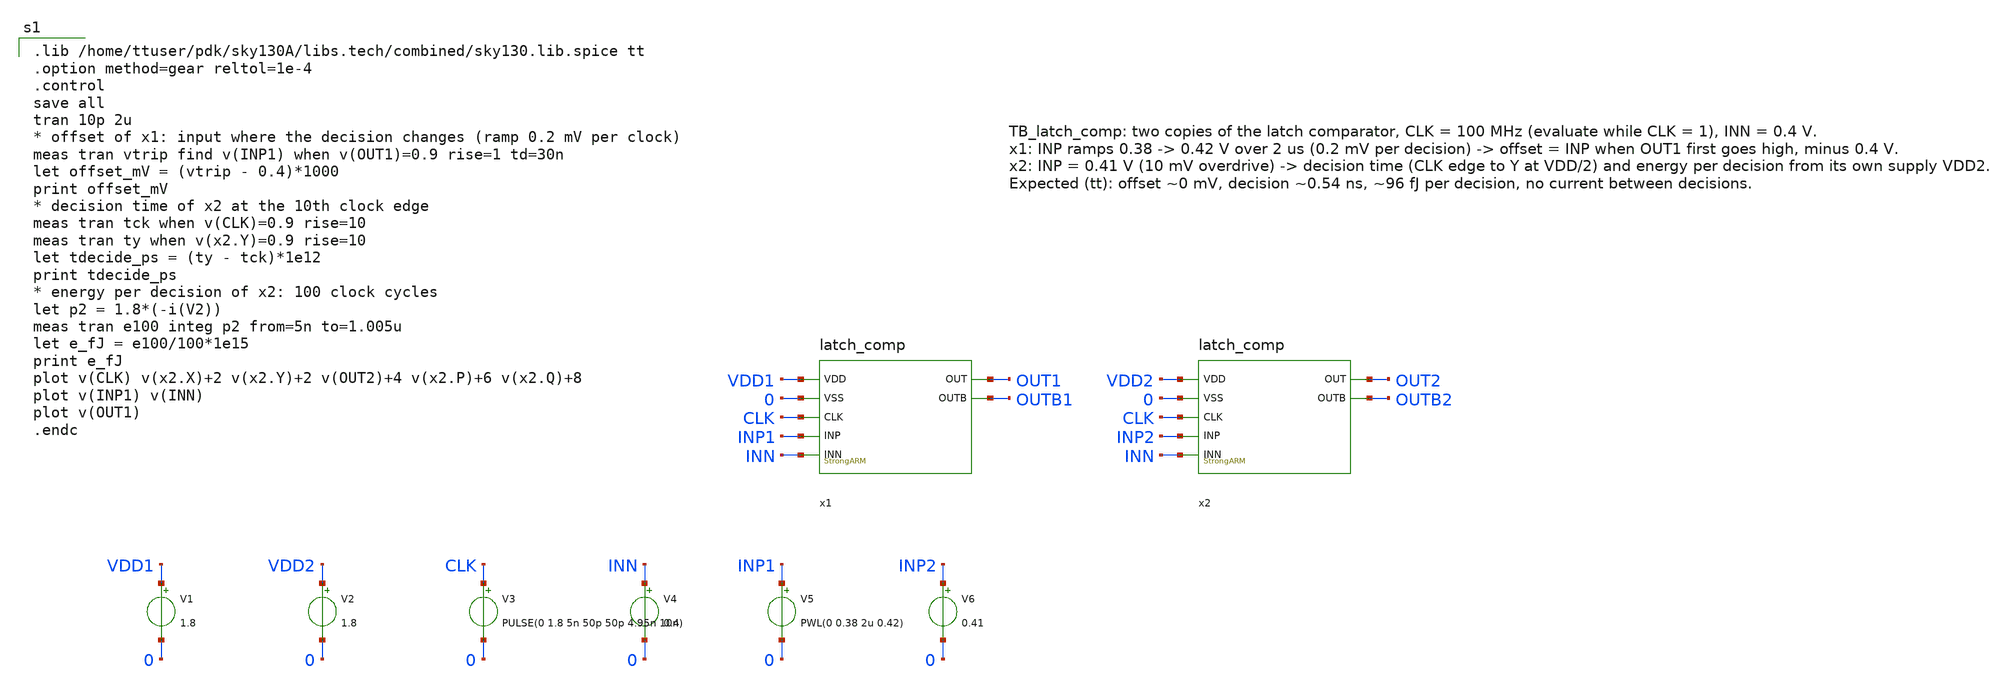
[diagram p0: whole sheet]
** sch_path: SAR_improved/TB_latch_comp.sch
**.subckt TB_latch_comp
x1 VDD1 0 CLK INP1 INN OUT1 OUTB1 latch_comp
x2 VDD2 0 CLK INP2 INN OUT2 OUTB2 latch_comp
V1 VDD1 0 1.8
V2 VDD2 0 1.8
V3 CLK 0 PULSE(0 1.8 5n 50p 50p 4.95n 10n)
V4 INN 0 0.4
V5 INP1 0 PWL(0 0.38 2u 0.42)
V6 INP2 0 0.41
**** begin user architecture code

.lib /home/ttuser/pdk/sky130A/libs.tech/combined/sky130.lib.spice tt
.option method=gear reltol=1e-4
.control
save all
tran 10p 2u
* offset of x1: input where the decision changes (ramp 0.2 mV per clock)
meas tran vtrip find v(INP1) when v(OUT1)=0.9 rise=1 td=30n
let offset_mV = (vtrip - 0.4)*1000
print offset_mV
* decision time of x2 at the 10th clock edge
meas tran tck when v(CLK)=0.9 rise=10
meas tran ty when v(x2.Y)=0.9 rise=10
let tdecide_ps = (ty - tck)*1e12
print tdecide_ps
* energy per decision of x2: 100 clock cycles
let p2 = 1.8*(-i(V2))
meas tran e100 integ p2 from=5n to=1.005u
let e_fJ = e100/100*1e15
print e_fJ
plot v(CLK) v(x2.X)+2 v(x2.Y)+2 v(OUT2)+4 v(x2.P)+6 v(x2.Q)+8
plot v(INP1) v(INN)
plot v(OUT1)
.endc

**** end user architecture code
**.ends

* expanding   symbol:  /home/ttuser/Documents/ADCAnalogDesign/SAR_improved/latch_comp.sym # of
*+ pins=7
** sym_path: SAR_improved/latch_comp.sym
** sch_path: SAR_improved/latch_comp.sch
.subckt latch_comp VDD VSS CLK INP INN OUT OUTB
*.ipin VDD
*.ipin VSS
*.ipin CLK
*.ipin INP
*.ipin INN
*.opin OUT
*.opin OUTB
XMCKP CLKB CLK VDD VDD sky130_fd_pr__pfet_01v8 L=0.15 W=1 nf=1 ad='int((nf+1)/2) * W/nf * 0.29' as='int((nf+2)/2) * W/nf * 0.29'
+ pd='2*int((nf+1)/2) * (W/nf + 0.29)' ps='2*int((nf+2)/2) * (W/nf + 0.29)' nrd='0.29 / W' nrs='0.29 / W'
+ sa=0 sb=0 sd=0 mult=1 m=1
XMCKN CLKB CLK VSS VSS sky130_fd_pr__nfet_01v8 L=0.15 W=0.5 nf=1 ad='int((nf+1)/2) * W/nf * 0.29' as='int((nf+2)/2) * W/nf * 0.29'
+ pd='2*int((nf+1)/2) * (W/nf + 0.29)' ps='2*int((nf+2)/2) * (W/nf + 0.29)' nrd='0.29 / W' nrs='0.29 / W'
+ sa=0 sb=0 sd=0 mult=1 m=1
XM7 TAIL CLKB VDD VDD sky130_fd_pr__pfet_01v8 L=0.15 W=2 nf=1 ad='int((nf+1)/2) * W/nf * 0.29' as='int((nf+2)/2) * W/nf * 0.29'
+ pd='2*int((nf+1)/2) * (W/nf + 0.29)' ps='2*int((nf+2)/2) * (W/nf + 0.29)' nrd='0.29 / W' nrs='0.29 / W'
+ sa=0 sb=0 sd=0 mult=1 m=1
XM1 P INP TAIL VDD sky130_fd_pr__pfet_01v8 L=0.5 W=2 nf=1 ad='int((nf+1)/2) * W/nf * 0.29' as='int((nf+2)/2) * W/nf * 0.29'
+ pd='2*int((nf+1)/2) * (W/nf + 0.29)' ps='2*int((nf+2)/2) * (W/nf + 0.29)' nrd='0.29 / W' nrs='0.29 / W'
+ sa=0 sb=0 sd=0 mult=1 m=1
XM2 Q INN TAIL VDD sky130_fd_pr__pfet_01v8 L=0.5 W=2 nf=1 ad='int((nf+1)/2) * W/nf * 0.29' as='int((nf+2)/2) * W/nf * 0.29'
+ pd='2*int((nf+1)/2) * (W/nf + 0.29)' ps='2*int((nf+2)/2) * (W/nf + 0.29)' nrd='0.29 / W' nrs='0.29 / W'
+ sa=0 sb=0 sd=0 mult=1 m=1
XM3 X Y P VDD sky130_fd_pr__pfet_01v8 L=0.15 W=1 nf=1 ad='int((nf+1)/2) * W/nf * 0.29' as='int((nf+2)/2) * W/nf * 0.29'
+ pd='2*int((nf+1)/2) * (W/nf + 0.29)' ps='2*int((nf+2)/2) * (W/nf + 0.29)' nrd='0.29 / W' nrs='0.29 / W'
+ sa=0 sb=0 sd=0 mult=1 m=1
XM4 Y X Q VDD sky130_fd_pr__pfet_01v8 L=0.15 W=1 nf=1 ad='int((nf+1)/2) * W/nf * 0.29' as='int((nf+2)/2) * W/nf * 0.29'
+ pd='2*int((nf+1)/2) * (W/nf + 0.29)' ps='2*int((nf+2)/2) * (W/nf + 0.29)' nrd='0.29 / W' nrs='0.29 / W'
+ sa=0 sb=0 sd=0 mult=1 m=1
XM5 X Y VSS VSS sky130_fd_pr__nfet_01v8 L=0.15 W=0.5 nf=1 ad='int((nf+1)/2) * W/nf * 0.29' as='int((nf+2)/2) * W/nf * 0.29'
+ pd='2*int((nf+1)/2) * (W/nf + 0.29)' ps='2*int((nf+2)/2) * (W/nf + 0.29)' nrd='0.29 / W' nrs='0.29 / W'
+ sa=0 sb=0 sd=0 mult=1 m=1
XM6 Y X VSS VSS sky130_fd_pr__nfet_01v8 L=0.15 W=0.5 nf=1 ad='int((nf+1)/2) * W/nf * 0.29' as='int((nf+2)/2) * W/nf * 0.29'
+ pd='2*int((nf+1)/2) * (W/nf + 0.29)' ps='2*int((nf+2)/2) * (W/nf + 0.29)' nrd='0.29 / W' nrs='0.29 / W'
+ sa=0 sb=0 sd=0 mult=1 m=1
XMR1 P CLKB VSS VSS sky130_fd_pr__nfet_01v8 L=0.15 W=0.5 nf=1 ad='int((nf+1)/2) * W/nf * 0.29' as='int((nf+2)/2) * W/nf * 0.29'
+ pd='2*int((nf+1)/2) * (W/nf + 0.29)' ps='2*int((nf+2)/2) * (W/nf + 0.29)' nrd='0.29 / W' nrs='0.29 / W'
+ sa=0 sb=0 sd=0 mult=1 m=1
XMR2 Q CLKB VSS VSS sky130_fd_pr__nfet_01v8 L=0.15 W=0.5 nf=1 ad='int((nf+1)/2) * W/nf * 0.29' as='int((nf+2)/2) * W/nf * 0.29'
+ pd='2*int((nf+1)/2) * (W/nf + 0.29)' ps='2*int((nf+2)/2) * (W/nf + 0.29)' nrd='0.29 / W' nrs='0.29 / W'
+ sa=0 sb=0 sd=0 mult=1 m=1
XMR3 X CLKB VSS VSS sky130_fd_pr__nfet_01v8 L=0.15 W=0.5 nf=1 ad='int((nf+1)/2) * W/nf * 0.29' as='int((nf+2)/2) * W/nf * 0.29'
+ pd='2*int((nf+1)/2) * (W/nf + 0.29)' ps='2*int((nf+2)/2) * (W/nf + 0.29)' nrd='0.29 / W' nrs='0.29 / W'
+ sa=0 sb=0 sd=0 mult=1 m=1
XMR4 Y CLKB VSS VSS sky130_fd_pr__nfet_01v8 L=0.15 W=0.5 nf=1 ad='int((nf+1)/2) * W/nf * 0.29' as='int((nf+2)/2) * W/nf * 0.29'
+ pd='2*int((nf+1)/2) * (W/nf + 0.29)' ps='2*int((nf+2)/2) * (W/nf + 0.29)' nrd='0.29 / W' nrs='0.29 / W'
+ sa=0 sb=0 sd=0 mult=1 m=1
XMBXP XB X VDD VDD sky130_fd_pr__pfet_01v8 L=0.15 W=1 nf=1 ad='int((nf+1)/2) * W/nf * 0.29' as='int((nf+2)/2) * W/nf * 0.29'
+ pd='2*int((nf+1)/2) * (W/nf + 0.29)' ps='2*int((nf+2)/2) * (W/nf + 0.29)' nrd='0.29 / W' nrs='0.29 / W'
+ sa=0 sb=0 sd=0 mult=1 m=1
XMBXN XB X VSS VSS sky130_fd_pr__nfet_01v8 L=0.15 W=0.5 nf=1 ad='int((nf+1)/2) * W/nf * 0.29' as='int((nf+2)/2) * W/nf * 0.29'
+ pd='2*int((nf+1)/2) * (W/nf + 0.29)' ps='2*int((nf+2)/2) * (W/nf + 0.29)' nrd='0.29 / W' nrs='0.29 / W'
+ sa=0 sb=0 sd=0 mult=1 m=1
XMBYP YB Y VDD VDD sky130_fd_pr__pfet_01v8 L=0.15 W=1 nf=1 ad='int((nf+1)/2) * W/nf * 0.29' as='int((nf+2)/2) * W/nf * 0.29'
+ pd='2*int((nf+1)/2) * (W/nf + 0.29)' ps='2*int((nf+2)/2) * (W/nf + 0.29)' nrd='0.29 / W' nrs='0.29 / W'
+ sa=0 sb=0 sd=0 mult=1 m=1
XMBYN YB Y VSS VSS sky130_fd_pr__nfet_01v8 L=0.15 W=0.5 nf=1 ad='int((nf+1)/2) * W/nf * 0.29' as='int((nf+2)/2) * W/nf * 0.29'
+ pd='2*int((nf+1)/2) * (W/nf + 0.29)' ps='2*int((nf+2)/2) * (W/nf + 0.29)' nrd='0.29 / W' nrs='0.29 / W'
+ sa=0 sb=0 sd=0 mult=1 m=1
x1 YB OUTB OUT VDD VSS nand2
x2 XB OUT OUTB VDD VSS nand2
.ends


* expanding   symbol:  /home/ttuser/Documents/ADCAnalogDesign/nand2.sym # of pins=5
** sym_path: SAR_improved/nand2.sym
** sch_path: SAR_improved/nand2.sch
.subckt nand2 A B Y VCC VSS
*.ipin A
*.ipin B
*.opin Y
*.iopin VCC
*.iopin VSS
XM1 Y A VCC VCC sky130_fd_pr__pfet_01v8 L=0.15 W=2 nf=1 ad='int((nf+1)/2) * W/nf * 0.29' as='int((nf+2)/2) * W/nf * 0.29'
+ pd='2*int((nf+1)/2) * (W/nf + 0.29)' ps='2*int((nf+2)/2) * (W/nf + 0.29)' nrd='0.29 / W' nrs='0.29 / W'
+ sa=0 sb=0 sd=0 mult=1 m=1
XM2 Y B VCC VCC sky130_fd_pr__pfet_01v8 L=0.15 W=2 nf=1 ad='int((nf+1)/2) * W/nf * 0.29' as='int((nf+2)/2) * W/nf * 0.29'
+ pd='2*int((nf+1)/2) * (W/nf + 0.29)' ps='2*int((nf+2)/2) * (W/nf + 0.29)' nrd='0.29 / W' nrs='0.29 / W'
+ sa=0 sb=0 sd=0 mult=1 m=1
XM3 Y A N1 VSS sky130_fd_pr__nfet_01v8 L=0.15 W=2 nf=1 ad='int((nf+1)/2) * W/nf * 0.29' as='int((nf+2)/2) * W/nf * 0.29'
+ pd='2*int((nf+1)/2) * (W/nf + 0.29)' ps='2*int((nf+2)/2) * (W/nf + 0.29)' nrd='0.29 / W' nrs='0.29 / W'
+ sa=0 sb=0 sd=0 mult=1 m=1
XM4 N1 B VSS VSS sky130_fd_pr__nfet_01v8 L=0.15 W=2 nf=1 ad='int((nf+1)/2) * W/nf * 0.29' as='int((nf+2)/2) * W/nf * 0.29'
+ pd='2*int((nf+1)/2) * (W/nf + 0.29)' ps='2*int((nf+2)/2) * (W/nf + 0.29)' nrd='0.29 / W' nrs='0.29 / W'
+ sa=0 sb=0 sd=0 mult=1 m=1
.ends

.end
